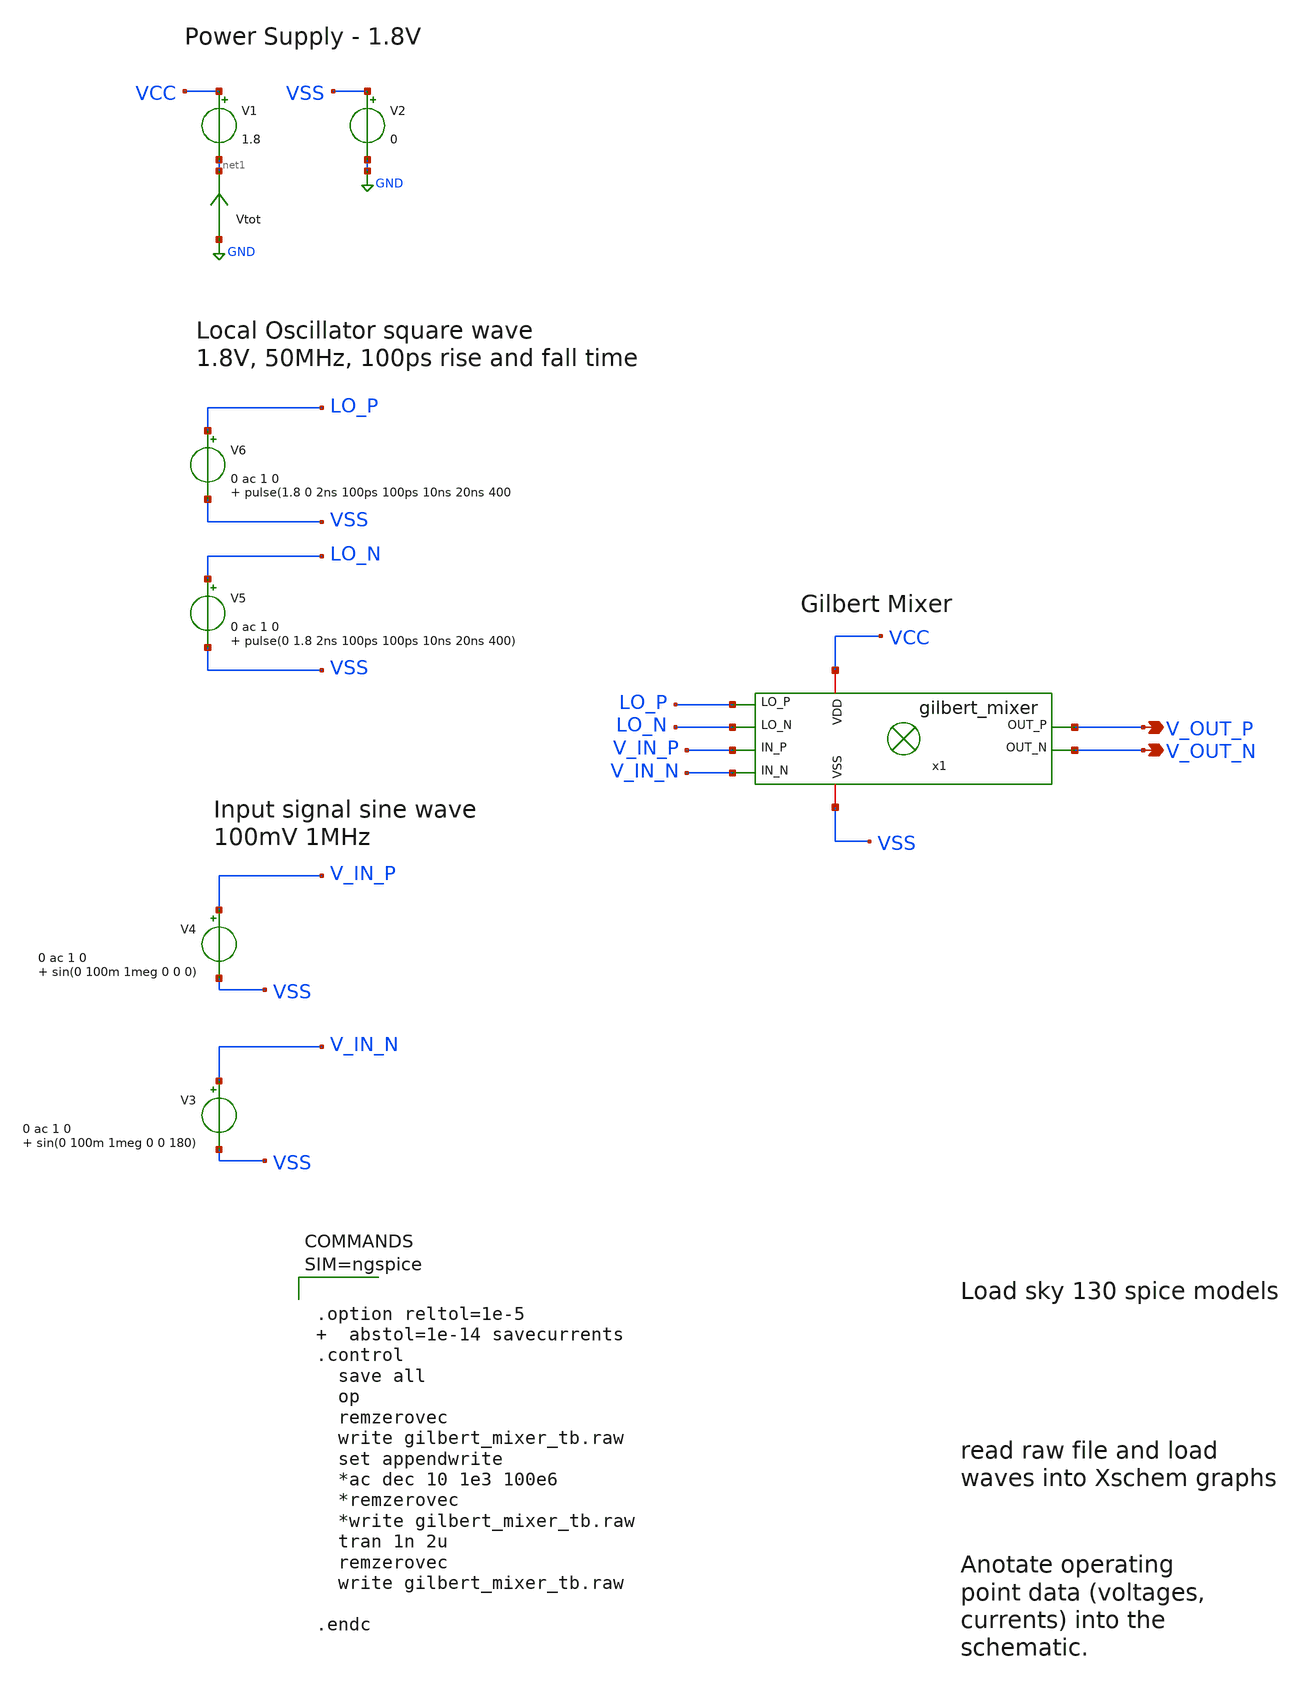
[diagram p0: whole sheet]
** sch_path: xschem/gilbert_mixer_tb.sch
**.subckt gilbert_mixer_tb V_OUT_N V_OUT_P
*.opin V_OUT_N
*.opin V_OUT_P
V1 VCC net1 1.8
V2 VSS GND 0
V4 V_IN_P VSS 0 ac 1 0 sin(0 100m 1meg 0 0 0)
x1 VSS VCC V_OUT_N V_OUT_P LO_N LO_P V_IN_N V_IN_P gilbert_mixer
V5 LO_N VSS 0 ac 1 0 pulse(0 1.8 2ns 100ps 100ps 10ns 20ns 400)
V3 V_IN_N VSS 0 ac 1 0 sin(0 100m 1meg 0 0 180)
Vtot GND net1 0
.save i(vtot)
V6 LO_P VSS 0 ac 1 0 pulse(1.8 0 2ns 100ps 100ps 10ns 20ns 400
**** begin user architecture code

** opencircuitdesign pdks install
.lib $::SKYWATER_MODELS/sky130.lib.spice tt





.option reltol=1e-5   abstol=1e-14 savecurrents
.control
  save all
  op
  remzerovec
  write gilbert_mixer_tb.raw
  set appendwrite
  *ac dec 10 1e3 100e6
  *remzerovec
  *write gilbert_mixer_tb.raw
  tran 1n 2u
  remzerovec
  write gilbert_mixer_tb.raw

.endc



**** end user architecture code
**.ends

* expanding   symbol:  gilbert_mixer.sym # of pins=8
** sym_path: xschem/gilbert_mixer.sym
** sch_path: xschem/gilbert_mixer.sch
.subckt gilbert_mixer VSS VDD OUT_N OUT_P LO_N LO_P IN_N IN_P
*.iopin VDD
*.iopin VSS
*.ipin LO_P
*.ipin LO_N
*.ipin IN_P
*.ipin IN_N
*.opin OUT_N
*.opin OUT_P
XR3 VSS NET_R3 net2 sky130_fd_pr__res_high_po_0p35 L=0.1 mult=15 m=15
XM2 OUT_P IN_N NET_M6_DRAIN VSS sky130_fd_pr__nfet_01v8 L=0.38 W=3.6 nf=2 ad='int((nf+1)/2) * W/nf * 0.29'
+ as='int((nf+2)/2) * W/nf * 0.29' pd='2*int((nf+1)/2) * (W/nf + 0.29)' ps='2*int((nf+2)/2) * (W/nf + 0.29)'
+ nrd='0.29 / W' nrs='0.29 / W' sa=0 sb=0 sd=0 mult=1 m=1
XM4 OUT_N IN_N NET_M5_DRAIN VSS sky130_fd_pr__nfet_01v8 L=0.38 W=3.6 nf=2 ad='int((nf+1)/2) * W/nf * 0.29'
+ as='int((nf+2)/2) * W/nf * 0.29' pd='2*int((nf+1)/2) * (W/nf + 0.29)' ps='2*int((nf+2)/2) * (W/nf + 0.29)'
+ nrd='0.29 / W' nrs='0.29 / W' sa=0 sb=0 sd=0 mult=1 m=1
XM6 NET_M6_DRAIN LO_N NET_R3 VSS sky130_fd_pr__nfet_01v8 L=0.38 W=3.6 nf=2 ad='int((nf+1)/2) * W/nf * 0.29'
+ as='int((nf+2)/2) * W/nf * 0.29' pd='2*int((nf+1)/2) * (W/nf + 0.29)' ps='2*int((nf+2)/2) * (W/nf + 0.29)'
+ nrd='0.29 / W' nrs='0.29 / W' sa=0 sb=0 sd=0 mult=1 m=1
XM1 OUT_N IN_P NET_M6_DRAIN VSS sky130_fd_pr__nfet_01v8 L=0.38 W=3.6 nf=2 ad='int((nf+1)/2) * W/nf * 0.29'
+ as='int((nf+2)/2) * W/nf * 0.29' pd='2*int((nf+1)/2) * (W/nf + 0.29)' ps='2*int((nf+2)/2) * (W/nf + 0.29)'
+ nrd='0.29 / W' nrs='0.29 / W' sa=0 sb=0 sd=0 mult=1 m=1
XM3 OUT_P IN_P NET_M5_DRAIN VSS sky130_fd_pr__nfet_01v8 L=0.38 W=3.6 nf=2 ad='int((nf+1)/2) * W/nf * 0.29'
+ as='int((nf+2)/2) * W/nf * 0.29' pd='2*int((nf+1)/2) * (W/nf + 0.29)' ps='2*int((nf+2)/2) * (W/nf + 0.29)'
+ nrd='0.29 / W' nrs='0.29 / W' sa=0 sb=0 sd=0 mult=1 m=1
XM5 NET_M5_DRAIN LO_P NET_R3 VSS sky130_fd_pr__nfet_01v8 L=0.38 W=3.6 nf=2 ad='int((nf+1)/2) * W/nf * 0.29'
+ as='int((nf+2)/2) * W/nf * 0.29' pd='2*int((nf+1)/2) * (W/nf + 0.29)' ps='2*int((nf+2)/2) * (W/nf + 0.29)'
+ nrd='0.29 / W' nrs='0.29 / W' sa=0 sb=0 sd=0 mult=1 m=1
XR2 OUT_P VDD net1 sky130_fd_pr__res_high_po_0p35 L=2.3 mult=1 m=1
XR1 OUT_N VDD VSS sky130_fd_pr__res_high_po_0p35 L=2.3 mult=1 m=1
.ends

.GLOBAL GND
.end
